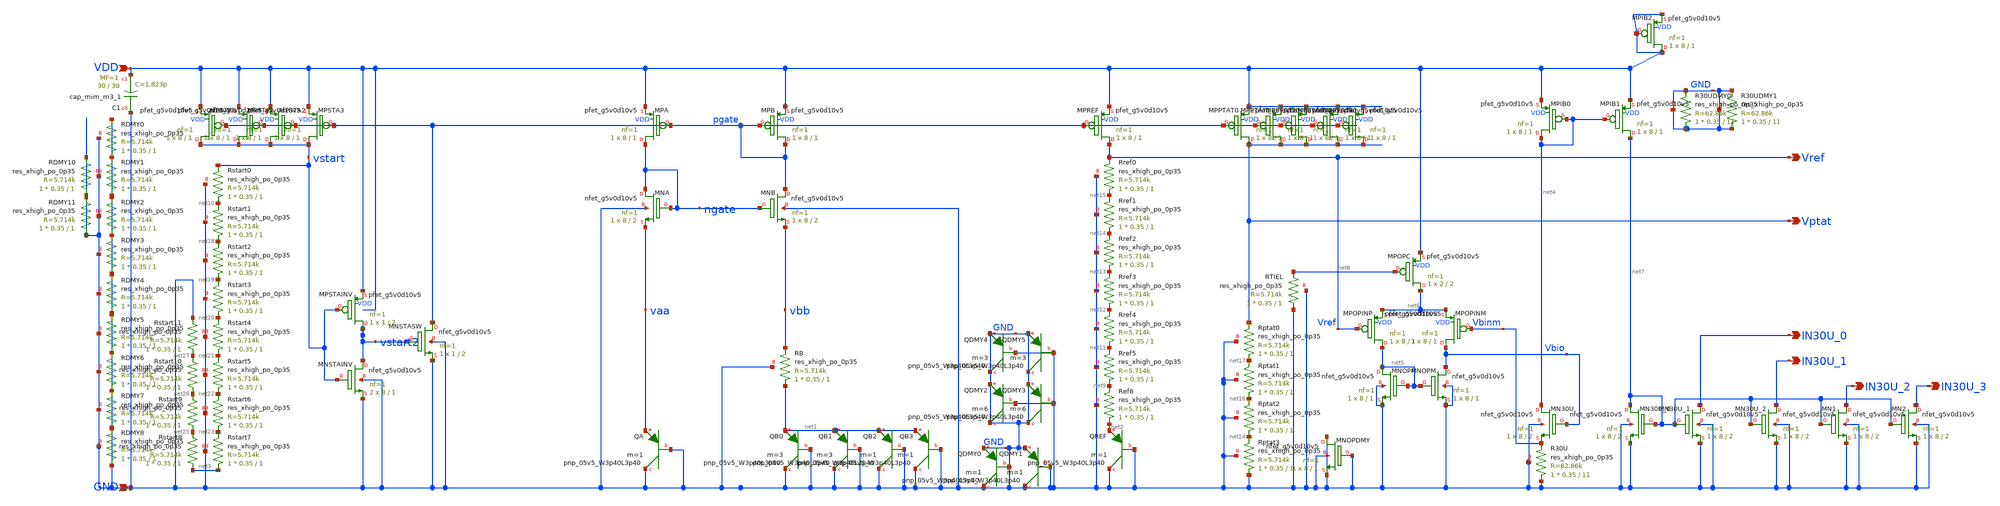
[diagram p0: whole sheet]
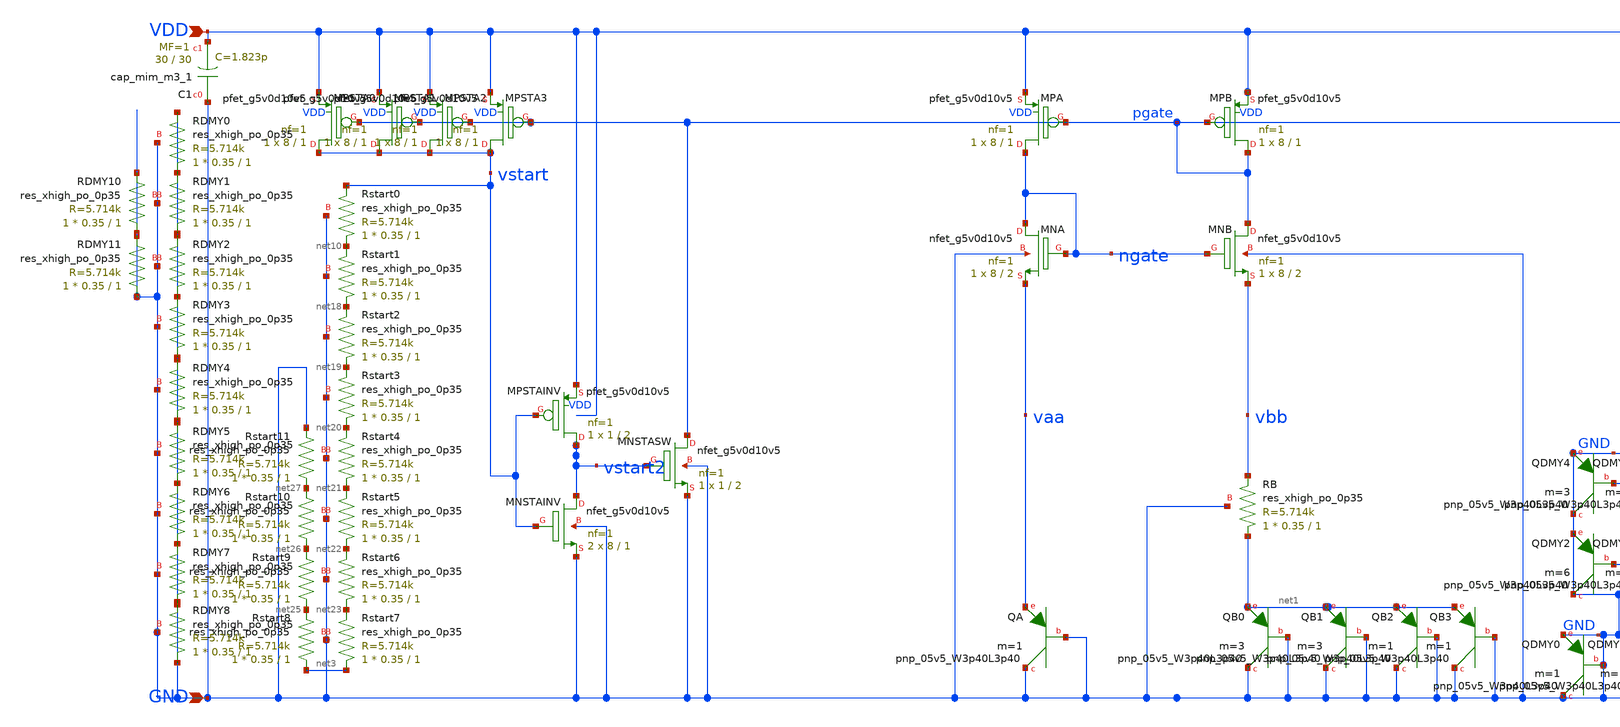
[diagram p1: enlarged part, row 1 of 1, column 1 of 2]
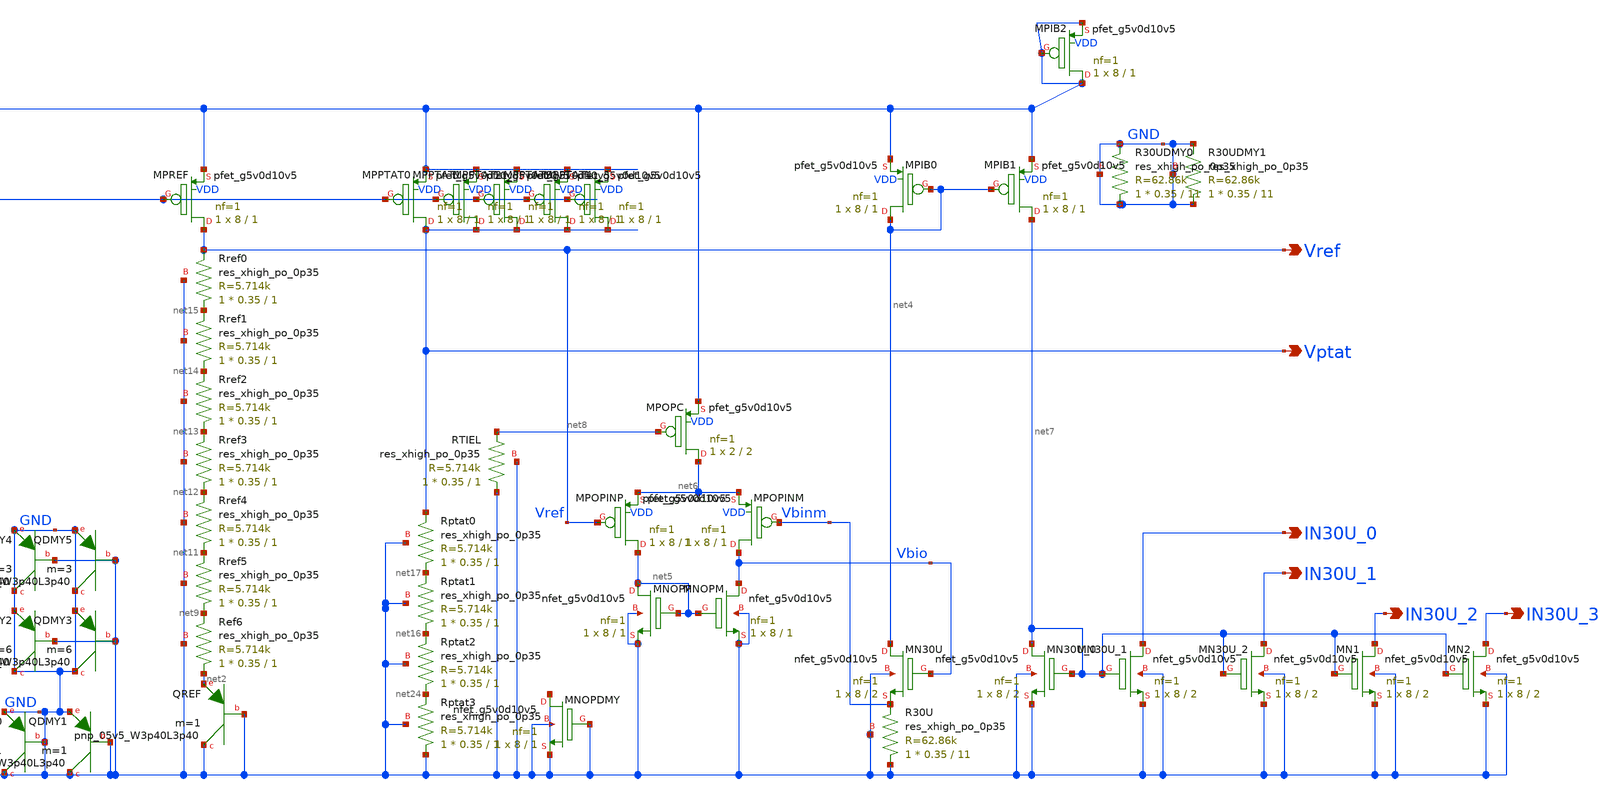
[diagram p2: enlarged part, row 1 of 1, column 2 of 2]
** sch_path: design/schematic/bgr3v3_v2.sch
**.subckt bgr3v3_v2 VDD GND Vref Vptat IN30U_0 IN30U_1 IN30U_2 IN30U_3
*.ipin VDD
*.ipin GND
*.opin Vref
*.opin Vptat
*.opin IN30U_0
*.opin IN30U_1
*.opin IN30U_2
*.opin IN30U_3
XQA GND GND vaa sky130_fd_pr__pnp_05v5_W3p40L3p40 m=1
XQB0 GND GND net1 sky130_fd_pr__pnp_05v5_W3p40L3p40 m=3
XRB net1 vbb GND sky130_fd_pr__res_xhigh_po_0p35 L=1 mult=1 m=1
XRef6 net2 net9 GND sky130_fd_pr__res_xhigh_po_0p35 L=1 mult=1 m=1
XQREF GND GND net2 sky130_fd_pr__pnp_05v5_W3p40L3p40 m=1
XqC1 GND VDD sky130_fd_pr__cap_mim_m3_1 W=30 L=30 MF=1 m=1
XRstart0 net10 vstart GND sky130_fd_pr__res_xhigh_po_0p35 L=1 mult=1 m=1
XRref5 net9 net11 GND sky130_fd_pr__res_xhigh_po_0p35 L=1 mult=1 m=1
XRref4 net11 net12 GND sky130_fd_pr__res_xhigh_po_0p35 L=1 mult=1 m=1
XRref3 net12 net13 GND sky130_fd_pr__res_xhigh_po_0p35 L=1 mult=1 m=1
XRref2 net13 net14 GND sky130_fd_pr__res_xhigh_po_0p35 L=1 mult=1 m=1
XRref1 net14 net15 GND sky130_fd_pr__res_xhigh_po_0p35 L=1 mult=1 m=1
XRref0 net15 Vref GND sky130_fd_pr__res_xhigh_po_0p35 L=1 mult=1 m=1
XRptat1 net16 net17 GND sky130_fd_pr__res_xhigh_po_0p35 L=1 mult=1 m=1
XRptat0 net17 Vptat GND sky130_fd_pr__res_xhigh_po_0p35 L=1 mult=1 m=1
XRstart1 net18 net10 GND sky130_fd_pr__res_xhigh_po_0p35 L=1 mult=1 m=1
XRstart2 net19 net18 GND sky130_fd_pr__res_xhigh_po_0p35 L=1 mult=1 m=1
XRstart3 net20 net19 GND sky130_fd_pr__res_xhigh_po_0p35 L=1 mult=1 m=1
XRstart4 net21 net20 GND sky130_fd_pr__res_xhigh_po_0p35 L=1 mult=1 m=1
XRstart5 net22 net21 GND sky130_fd_pr__res_xhigh_po_0p35 L=1 mult=1 m=1
XRstart6 net23 net22 GND sky130_fd_pr__res_xhigh_po_0p35 L=1 mult=1 m=1
XRstart7 net3 net23 GND sky130_fd_pr__res_xhigh_po_0p35 L=1 mult=1 m=1
XQB1 GND GND net1 sky130_fd_pr__pnp_05v5_W3p40L3p40 m=3
XQB2 GND GND net1 sky130_fd_pr__pnp_05v5_W3p40L3p40 m=1
XQB3 GND GND net1 sky130_fd_pr__pnp_05v5_W3p40L3p40 m=1
XQDMY0 GND GND GND sky130_fd_pr__pnp_05v5_W3p40L3p40 m=1
XQDMY1 GND GND GND sky130_fd_pr__pnp_05v5_W3p40L3p40 m=1
XRptat2 net24 net16 GND sky130_fd_pr__res_xhigh_po_0p35 L=1 mult=1 m=1
XRstart8 net3 net25 GND sky130_fd_pr__res_xhigh_po_0p35 L=1 mult=1 m=1
XRstart9 net25 net26 GND sky130_fd_pr__res_xhigh_po_0p35 L=1 mult=1 m=1
XRstart10 net26 net27 GND sky130_fd_pr__res_xhigh_po_0p35 L=1 mult=1 m=1
XRstart11 net27 GND GND sky130_fd_pr__res_xhigh_po_0p35 L=1 mult=1 m=1
XMPREF Vref pgate VDD VDD sky130_fd_pr__pfet_g5v0d10v5 L=1 W=8 nf=1 ad='int((nf+1)/2) * W/nf * 0.29'
+ as='int((nf+2)/2) * W/nf * 0.29' pd='2*int((nf+1)/2) * (W/nf + 0.29)' ps='2*int((nf+2)/2) * (W/nf + 0.29)'
+ nrd='0.29 / W' nrs='0.29 / W' sa=0 sb=0 sd=0 mult=1 m=1
XMPB pgate pgate VDD VDD sky130_fd_pr__pfet_g5v0d10v5 L=1 W=8 nf=1 ad='int((nf+1)/2) * W/nf * 0.29' as='int((nf+2)/2) * W/nf * 0.29'
+ pd='2*int((nf+1)/2) * (W/nf + 0.29)' ps='2*int((nf+2)/2) * (W/nf + 0.29)' nrd='0.29 / W' nrs='0.29 / W'
+ sa=0 sb=0 sd=0 mult=1 m=1
XMPA ngate pgate VDD VDD sky130_fd_pr__pfet_g5v0d10v5 L=1 W=8 nf=1 ad='int((nf+1)/2) * W/nf * 0.29' as='int((nf+2)/2) * W/nf * 0.29'
+ pd='2*int((nf+1)/2) * (W/nf + 0.29)' ps='2*int((nf+2)/2) * (W/nf + 0.29)' nrd='0.29 / W' nrs='0.29 / W'
+ sa=0 sb=0 sd=0 mult=1 m=1
XMPPTAT0 Vptat pgate VDD VDD sky130_fd_pr__pfet_g5v0d10v5 L=1 W=8 nf=1 ad='int((nf+1)/2) * W/nf * 0.29'
+ as='int((nf+2)/2) * W/nf * 0.29' pd='2*int((nf+1)/2) * (W/nf + 0.29)' ps='2*int((nf+2)/2) * (W/nf + 0.29)'
+ nrd='0.29 / W' nrs='0.29 / W' sa=0 sb=0 sd=0 mult=1 m=1
XMNB pgate ngate vbb GND sky130_fd_pr__nfet_g5v0d10v5 L=2 W=8 nf=1 ad='int((nf+1)/2) * W/nf * 0.29' as='int((nf+2)/2) * W/nf * 0.29'
+ pd='2*int((nf+1)/2) * (W/nf + 0.29)' ps='2*int((nf+2)/2) * (W/nf + 0.29)' nrd='0.29 / W' nrs='0.29 / W'
+ sa=0 sb=0 sd=0 mult=1 m=1
XMNA ngate ngate vaa GND sky130_fd_pr__nfet_g5v0d10v5 L=2 W=8 nf=1 ad='int((nf+1)/2) * W/nf * 0.29' as='int((nf+2)/2) * W/nf * 0.29'
+ pd='2*int((nf+1)/2) * (W/nf + 0.29)' ps='2*int((nf+2)/2) * (W/nf + 0.29)' nrd='0.29 / W' nrs='0.29 / W'
+ sa=0 sb=0 sd=0 mult=1 m=1
XMNSTASW pgate vstart2 GND GND sky130_fd_pr__nfet_g5v0d10v5 L=2 W=1 nf=1 ad='int((nf+1)/2) * W/nf * 0.29'
+ as='int((nf+2)/2) * W/nf * 0.29' pd='2*int((nf+1)/2) * (W/nf + 0.29)' ps='2*int((nf+2)/2) * (W/nf + 0.29)'
+ nrd='0.29 / W' nrs='0.29 / W' sa=0 sb=0 sd=0 mult=1 m=1
XMNSTAINV vstart2 vstart GND GND sky130_fd_pr__nfet_g5v0d10v5 L=1 W=8 nf=1 ad='int((nf+1)/2) * W/nf * 0.29'
+ as='int((nf+2)/2) * W/nf * 0.29' pd='2*int((nf+1)/2) * (W/nf + 0.29)' ps='2*int((nf+2)/2) * (W/nf + 0.29)'
+ nrd='0.29 / W' nrs='0.29 / W' sa=0 sb=0 sd=0 mult=2 m=2
XMPSTAINV vstart2 vstart VDD VDD sky130_fd_pr__pfet_g5v0d10v5 L=2 W=1 nf=1 ad='int((nf+1)/2) * W/nf * 0.29'
+ as='int((nf+2)/2) * W/nf * 0.29' pd='2*int((nf+1)/2) * (W/nf + 0.29)' ps='2*int((nf+2)/2) * (W/nf + 0.29)'
+ nrd='0.29 / W' nrs='0.29 / W' sa=0 sb=0 sd=0 mult=1 m=1
XR30U GND Vbinm GND sky130_fd_pr__res_xhigh_po_0p35 L=11 mult=1 m=1
XMN30U net4 Vbio Vbinm GND sky130_fd_pr__nfet_g5v0d10v5 L=2 W=8 nf=1 ad='int((nf+1)/2) * W/nf * 0.29'
+ as='int((nf+2)/2) * W/nf * 0.29' pd='2*int((nf+1)/2) * (W/nf + 0.29)' ps='2*int((nf+2)/2) * (W/nf + 0.29)'
+ nrd='0.29 / W' nrs='0.29 / W' sa=0 sb=0 sd=0 mult=1 m=1
XMN30U_0 net7 net7 GND GND sky130_fd_pr__nfet_g5v0d10v5 L=2 W=8 nf=1 ad='int((nf+1)/2) * W/nf * 0.29'
+ as='int((nf+2)/2) * W/nf * 0.29' pd='2*int((nf+1)/2) * (W/nf + 0.29)' ps='2*int((nf+2)/2) * (W/nf + 0.29)'
+ nrd='0.29 / W' nrs='0.29 / W' sa=0 sb=0 sd=0 mult=1 m=1
XMNOPM Vbio net5 GND GND sky130_fd_pr__nfet_g5v0d10v5 L=1 W=8 nf=1 ad='int((nf+1)/2) * W/nf * 0.29' as='int((nf+2)/2) * W/nf * 0.29'
+ pd='2*int((nf+1)/2) * (W/nf + 0.29)' ps='2*int((nf+2)/2) * (W/nf + 0.29)' nrd='0.29 / W' nrs='0.29 / W'
+ sa=0 sb=0 sd=0 mult=1 m=1
XMNOPP net5 net5 GND GND sky130_fd_pr__nfet_g5v0d10v5 L=1 W=8 nf=1 ad='int((nf+1)/2) * W/nf * 0.29' as='int((nf+2)/2) * W/nf * 0.29'
+ pd='2*int((nf+1)/2) * (W/nf + 0.29)' ps='2*int((nf+2)/2) * (W/nf + 0.29)' nrd='0.29 / W' nrs='0.29 / W'
+ sa=0 sb=0 sd=0 mult=1 m=1
XMPOPINP net5 Vref net6 VDD sky130_fd_pr__pfet_g5v0d10v5 L=1 W=8 nf=1 ad='int((nf+1)/2) * W/nf * 0.29'
+ as='int((nf+2)/2) * W/nf * 0.29' pd='2*int((nf+1)/2) * (W/nf + 0.29)' ps='2*int((nf+2)/2) * (W/nf + 0.29)'
+ nrd='0.29 / W' nrs='0.29 / W' sa=0 sb=0 sd=0 mult=1 m=1
XMPOPINM Vbio Vbinm net6 VDD sky130_fd_pr__pfet_g5v0d10v5 L=1 W=8 nf=1 ad='int((nf+1)/2) * W/nf * 0.29'
+ as='int((nf+2)/2) * W/nf * 0.29' pd='2*int((nf+1)/2) * (W/nf + 0.29)' ps='2*int((nf+2)/2) * (W/nf + 0.29)'
+ nrd='0.29 / W' nrs='0.29 / W' sa=0 sb=0 sd=0 mult=1 m=1
XMPOPC net6 net8 VDD VDD sky130_fd_pr__pfet_g5v0d10v5 L=2 W=2 nf=1 ad='int((nf+1)/2) * W/nf * 0.29' as='int((nf+2)/2) * W/nf * 0.29'
+ pd='2*int((nf+1)/2) * (W/nf + 0.29)' ps='2*int((nf+2)/2) * (W/nf + 0.29)' nrd='0.29 / W' nrs='0.29 / W'
+ sa=0 sb=0 sd=0 mult=1 m=1
XMPSTA0 vstart pgate VDD VDD sky130_fd_pr__pfet_g5v0d10v5 L=1 W=8 nf=1 ad='int((nf+1)/2) * W/nf * 0.29'
+ as='int((nf+2)/2) * W/nf * 0.29' pd='2*int((nf+1)/2) * (W/nf + 0.29)' ps='2*int((nf+2)/2) * (W/nf + 0.29)'
+ nrd='0.29 / W' nrs='0.29 / W' sa=0 sb=0 sd=0 mult=1 m=1
XRptat3 GND net24 GND sky130_fd_pr__res_xhigh_po_0p35 L=1 mult=1 m=1
XMPPTAT1 Vptat pgate VDD VDD sky130_fd_pr__pfet_g5v0d10v5 L=1 W=8 nf=1 ad='int((nf+1)/2) * W/nf * 0.29'
+ as='int((nf+2)/2) * W/nf * 0.29' pd='2*int((nf+1)/2) * (W/nf + 0.29)' ps='2*int((nf+2)/2) * (W/nf + 0.29)'
+ nrd='0.29 / W' nrs='0.29 / W' sa=0 sb=0 sd=0 mult=1 m=1
XMPPTAT2 Vptat pgate VDD VDD sky130_fd_pr__pfet_g5v0d10v5 L=1 W=8 nf=1 ad='int((nf+1)/2) * W/nf * 0.29'
+ as='int((nf+2)/2) * W/nf * 0.29' pd='2*int((nf+1)/2) * (W/nf + 0.29)' ps='2*int((nf+2)/2) * (W/nf + 0.29)'
+ nrd='0.29 / W' nrs='0.29 / W' sa=0 sb=0 sd=0 mult=1 m=1
XMPPTAT3 Vptat pgate VDD VDD sky130_fd_pr__pfet_g5v0d10v5 L=1 W=8 nf=1 ad='int((nf+1)/2) * W/nf * 0.29'
+ as='int((nf+2)/2) * W/nf * 0.29' pd='2*int((nf+1)/2) * (W/nf + 0.29)' ps='2*int((nf+2)/2) * (W/nf + 0.29)'
+ nrd='0.29 / W' nrs='0.29 / W' sa=0 sb=0 sd=0 mult=1 m=1
XMPPTAT4 Vptat pgate VDD VDD sky130_fd_pr__pfet_g5v0d10v5 L=1 W=8 nf=1 ad='int((nf+1)/2) * W/nf * 0.29'
+ as='int((nf+2)/2) * W/nf * 0.29' pd='2*int((nf+1)/2) * (W/nf + 0.29)' ps='2*int((nf+2)/2) * (W/nf + 0.29)'
+ nrd='0.29 / W' nrs='0.29 / W' sa=0 sb=0 sd=0 mult=1 m=1
XMPSTA1 vstart pgate VDD VDD sky130_fd_pr__pfet_g5v0d10v5 L=1 W=8 nf=1 ad='int((nf+1)/2) * W/nf * 0.29'
+ as='int((nf+2)/2) * W/nf * 0.29' pd='2*int((nf+1)/2) * (W/nf + 0.29)' ps='2*int((nf+2)/2) * (W/nf + 0.29)'
+ nrd='0.29 / W' nrs='0.29 / W' sa=0 sb=0 sd=0 mult=1 m=1
XMPSTA2 vstart pgate VDD VDD sky130_fd_pr__pfet_g5v0d10v5 L=1 W=8 nf=1 ad='int((nf+1)/2) * W/nf * 0.29'
+ as='int((nf+2)/2) * W/nf * 0.29' pd='2*int((nf+1)/2) * (W/nf + 0.29)' ps='2*int((nf+2)/2) * (W/nf + 0.29)'
+ nrd='0.29 / W' nrs='0.29 / W' sa=0 sb=0 sd=0 mult=1 m=1
XMPSTA3 vstart pgate VDD VDD sky130_fd_pr__pfet_g5v0d10v5 L=1 W=8 nf=1 ad='int((nf+1)/2) * W/nf * 0.29'
+ as='int((nf+2)/2) * W/nf * 0.29' pd='2*int((nf+1)/2) * (W/nf + 0.29)' ps='2*int((nf+2)/2) * (W/nf + 0.29)'
+ nrd='0.29 / W' nrs='0.29 / W' sa=0 sb=0 sd=0 mult=1 m=1
XMN30U_1 IN30U_0 net7 GND GND sky130_fd_pr__nfet_g5v0d10v5 L=2 W=8 nf=1 ad='int((nf+1)/2) * W/nf * 0.29'
+ as='int((nf+2)/2) * W/nf * 0.29' pd='2*int((nf+1)/2) * (W/nf + 0.29)' ps='2*int((nf+2)/2) * (W/nf + 0.29)'
+ nrd='0.29 / W' nrs='0.29 / W' sa=0 sb=0 sd=0 mult=1 m=1
XMN30U_2 IN30U_1 net7 GND GND sky130_fd_pr__nfet_g5v0d10v5 L=2 W=8 nf=1 ad='int((nf+1)/2) * W/nf * 0.29'
+ as='int((nf+2)/2) * W/nf * 0.29' pd='2*int((nf+1)/2) * (W/nf + 0.29)' ps='2*int((nf+2)/2) * (W/nf + 0.29)'
+ nrd='0.29 / W' nrs='0.29 / W' sa=0 sb=0 sd=0 mult=1 m=1
XQDMY2 GND GND GND sky130_fd_pr__pnp_05v5_W3p40L3p40 m=6
XQDMY3 GND GND GND sky130_fd_pr__pnp_05v5_W3p40L3p40 m=6
XQDMY4 GND GND GND sky130_fd_pr__pnp_05v5_W3p40L3p40 m=3
XQDMY5 GND GND GND sky130_fd_pr__pnp_05v5_W3p40L3p40 m=3
XMNOPDMY GND GND GND GND sky130_fd_pr__nfet_g5v0d10v5 L=1 W=8 nf=1 ad='int((nf+1)/2) * W/nf * 0.29' as='int((nf+2)/2) * W/nf * 0.29'
+ pd='2*int((nf+1)/2) * (W/nf + 0.29)' ps='2*int((nf+2)/2) * (W/nf + 0.29)' nrd='0.29 / W' nrs='0.29 / W'
+ sa=0 sb=0 sd=0 mult=1 m=1
XRDMY0 GND GND GND sky130_fd_pr__res_xhigh_po_0p35 L=1 mult=1 m=1
XRDMY1 GND GND GND sky130_fd_pr__res_xhigh_po_0p35 L=1 mult=1 m=1
XRDMY2 GND GND GND sky130_fd_pr__res_xhigh_po_0p35 L=1 mult=1 m=1
XRDMY3 GND GND GND sky130_fd_pr__res_xhigh_po_0p35 L=1 mult=1 m=1
XRDMY4 GND GND GND sky130_fd_pr__res_xhigh_po_0p35 L=1 mult=1 m=1
XRDMY5 GND GND GND sky130_fd_pr__res_xhigh_po_0p35 L=1 mult=1 m=1
XRDMY6 GND GND GND sky130_fd_pr__res_xhigh_po_0p35 L=1 mult=1 m=1
XRDMY7 GND GND GND sky130_fd_pr__res_xhigh_po_0p35 L=1 mult=1 m=1
XRDMY8 GND GND GND sky130_fd_pr__res_xhigh_po_0p35 L=1 mult=1 m=1
XR30UDMY0 GND GND GND sky130_fd_pr__res_xhigh_po_0p35 L=11 mult=1 m=1
XR30UDMY1 GND GND GND sky130_fd_pr__res_xhigh_po_0p35 L=11 mult=1 m=1
XRTIEL GND net8 GND sky130_fd_pr__res_xhigh_po_0p35 L=1 mult=1 m=1
XRDMY10 GND GND GND sky130_fd_pr__res_xhigh_po_0p35 L=1 mult=1 m=1
XRDMY11 GND GND GND sky130_fd_pr__res_xhigh_po_0p35 L=1 mult=1 m=1
XMPIB0 net4 net4 VDD VDD sky130_fd_pr__pfet_g5v0d10v5 L=1 W=8 nf=1 ad='int((nf+1)/2) * W/nf * 0.29' as='int((nf+2)/2) * W/nf * 0.29'
+ pd='2*int((nf+1)/2) * (W/nf + 0.29)' ps='2*int((nf+2)/2) * (W/nf + 0.29)' nrd='0.29 / W' nrs='0.29 / W'
+ sa=0 sb=0 sd=0 mult=1 m=1
XMPIB1 net7 net4 VDD VDD sky130_fd_pr__pfet_g5v0d10v5 L=1 W=8 nf=1 ad='int((nf+1)/2) * W/nf * 0.29' as='int((nf+2)/2) * W/nf * 0.29'
+ pd='2*int((nf+1)/2) * (W/nf + 0.29)' ps='2*int((nf+2)/2) * (W/nf + 0.29)' nrd='0.29 / W' nrs='0.29 / W'
+ sa=0 sb=0 sd=0 mult=1 m=1
XMPIB2 VDD VDD VDD VDD sky130_fd_pr__pfet_g5v0d10v5 L=1 W=8 nf=1 ad='int((nf+1)/2) * W/nf * 0.29' as='int((nf+2)/2) * W/nf * 0.29'
+ pd='2*int((nf+1)/2) * (W/nf + 0.29)' ps='2*int((nf+2)/2) * (W/nf + 0.29)' nrd='0.29 / W' nrs='0.29 / W'
+ sa=0 sb=0 sd=0 mult=1 m=1
XMN1 IN30U_2 net7 GND GND sky130_fd_pr__nfet_g5v0d10v5 L=2 W=8 nf=1 ad='int((nf+1)/2) * W/nf * 0.29'
+ as='int((nf+2)/2) * W/nf * 0.29' pd='2*int((nf+1)/2) * (W/nf + 0.29)' ps='2*int((nf+2)/2) * (W/nf + 0.29)'
+ nrd='0.29 / W' nrs='0.29 / W' sa=0 sb=0 sd=0 mult=1 m=1
XMN2 IN30U_3 net7 GND GND sky130_fd_pr__nfet_g5v0d10v5 L=2 W=8 nf=1 ad='int((nf+1)/2) * W/nf * 0.29'
+ as='int((nf+2)/2) * W/nf * 0.29' pd='2*int((nf+1)/2) * (W/nf + 0.29)' ps='2*int((nf+2)/2) * (W/nf + 0.29)'
+ nrd='0.29 / W' nrs='0.29 / W' sa=0 sb=0 sd=0 mult=1 m=1
**.ends
.end
